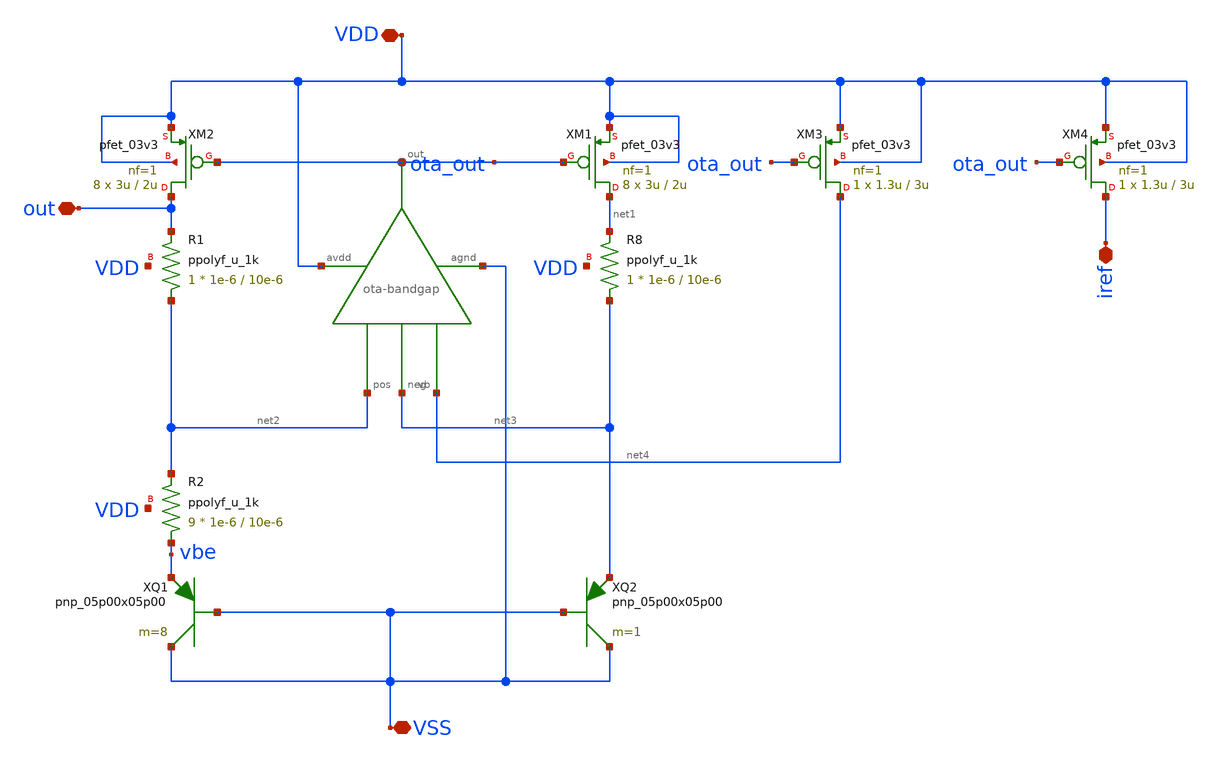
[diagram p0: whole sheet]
** sch_path: LDO/xschem/bandgap/symbol/bandgap_prev.sch

.include $env(PDK_ROOT)/$env(PDK)/libs.tech/ngspice/design.ngspice
.lib $env(PDK_ROOT)/$env(PDK)/libs.tech/ngspice/sm141064.ngspice typical
.lib $env(PDK_ROOT)/$env(PDK)/libs.tech/ngspice/sm141064.ngspice mimcap_statistical
.lib $env(PDK_ROOT)/$env(PDK)/libs.tech/ngspice/sm141064.ngspice cap_mim
.lib $env(PDK_ROOT)/$env(PDK)/libs.tech/ngspice/sm141064.ngspice res_typical
.lib $env(PDK_ROOT)/$env(PDK)/libs.tech/ngspice/sm141064.ngspice bjt_typical
.lib $env(PDK_ROOT)/$env(PDK)/libs.tech/ngspice/sm141064.ngspice moscap_typical

**.subckt bandgap_prev VDD VSS out iref
*.iopin VDD
*.iopin VSS
*.iopin out
*.iopin iref
XM1 net1 ota_out VDD VDD pfet_03v3 L=2u W=3u nf=1 ad='int((nf+1)/2) * W/nf * 0.18u' as='int((nf+2)/2) * W/nf * 0.18u'
+ pd='2*int((nf+1)/2) * (W/nf + 0.18u)' ps='2*int((nf+2)/2) * (W/nf + 0.18u)' nrd='0.18u / W' nrs='0.18u / W'
+ sa=0 sb=0 sd=0 m=8
XM2 out ota_out VDD VDD pfet_03v3 L=2u W=3u nf=1 ad='int((nf+1)/2) * W/nf * 0.18u' as='int((nf+2)/2) * W/nf * 0.18u'
+ pd='2*int((nf+1)/2) * (W/nf + 0.18u)' ps='2*int((nf+2)/2) * (W/nf + 0.18u)' nrd='0.18u / W' nrs='0.18u / W'
+ sa=0 sb=0 sd=0 m=8
X1 ota_out VSS VDD net2 net3 net4 ota-bandgap
XQ1 VSS VSS vbe pnp_05p00x05p00 m=8
XQ2 VSS VSS net3 pnp_05p00x05p00 m=1
XR8 net3 net1 VDD ppolyf_u_1k r_width=1e-6 r_length=10e-6 m=1
XR1 net2 out VDD ppolyf_u_1k r_width=1e-6 r_length=10e-6 m=1
XR2 vbe net2 VDD ppolyf_u_1k r_width=1e-6 r_length=10e-6 m=9
XM3 net4 ota_out VDD VDD pfet_03v3 L=3u W=1.3u nf=1 ad='int((nf+1)/2) * W/nf * 0.18u' as='int((nf+2)/2) * W/nf * 0.18u'
+ pd='2*int((nf+1)/2) * (W/nf + 0.18u)' ps='2*int((nf+2)/2) * (W/nf + 0.18u)' nrd='0.18u / W' nrs='0.18u / W'
+ sa=0 sb=0 sd=0 m=1
XM4 iref ota_out VDD VDD pfet_03v3 L=3u W=1.3u nf=1 ad='int((nf+1)/2) * W/nf * 0.18u' as='int((nf+2)/2) * W/nf * 0.18u'
+ pd='2*int((nf+1)/2) * (W/nf + 0.18u)' ps='2*int((nf+2)/2) * (W/nf + 0.18u)' nrd='0.18u / W' nrs='0.18u / W'
+ sa=0 sb=0 sd=0 m=1
**.ends
.end
